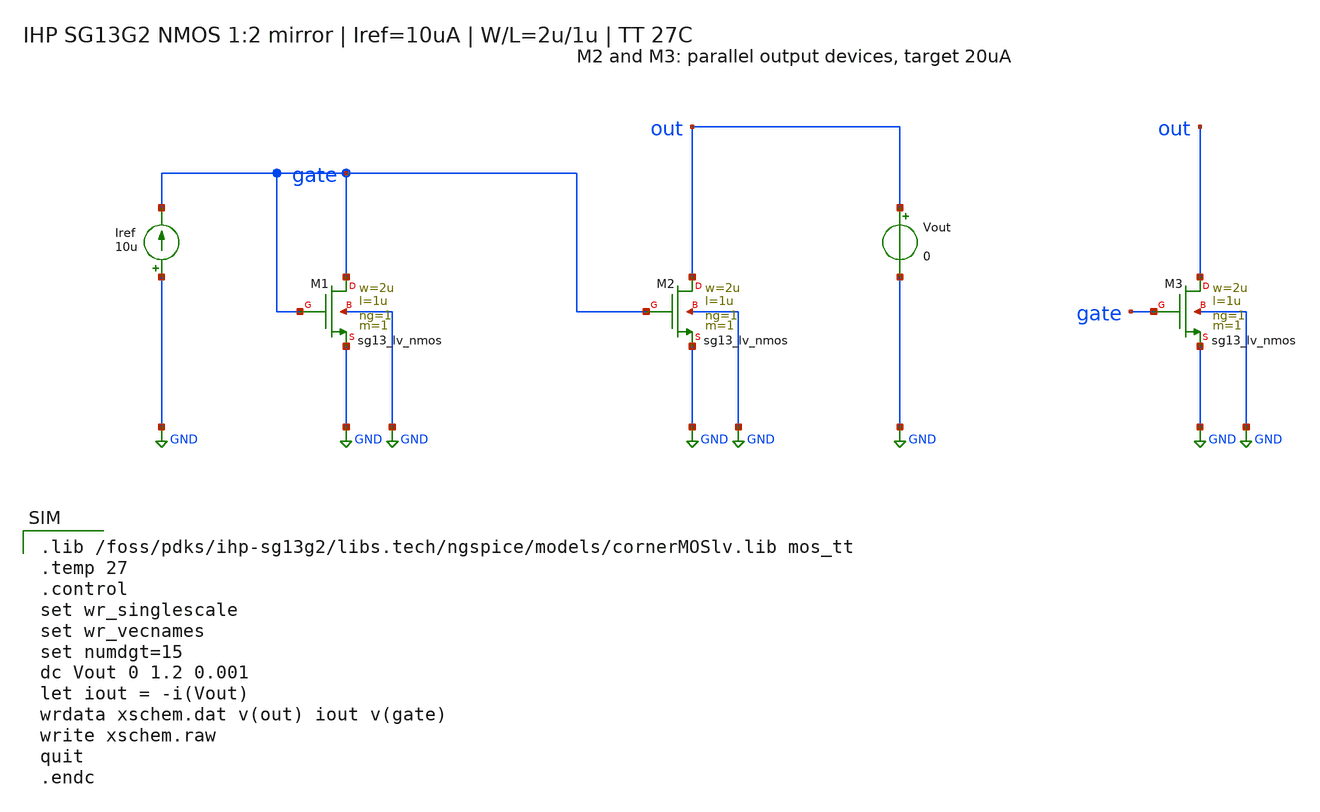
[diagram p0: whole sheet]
** sch_path: designs/first_ic/current_mirror/mirror_1to2/mirror_1to2.sch
**.subckt mirror_1to2
XM1 gate gate GND GND sg13_lv_nmos w=2u l=1u ng=1 m=1 mm_ok=0
XM2 out gate GND GND sg13_lv_nmos w=2u l=1u ng=1 m=1 mm_ok=0
Iref GND gate 10u
Vout out GND 0
XM3 out gate GND GND sg13_lv_nmos w=2u l=1u ng=1 m=1 mm_ok=0
**** begin user architecture code

.lib /foss/pdks/ihp-sg13g2/libs.tech/ngspice/models/cornerMOSlv.lib mos_tt
.temp 27
.control
set wr_singlescale
set wr_vecnames
set numdgt=15
dc Vout 0 1.2 0.001
let iout = -i(Vout)
wrdata xschem.dat v(out) iout v(gate)
write xschem.raw
quit
.endc


**** end user architecture code
**.ends
.GLOBAL GND
.end
